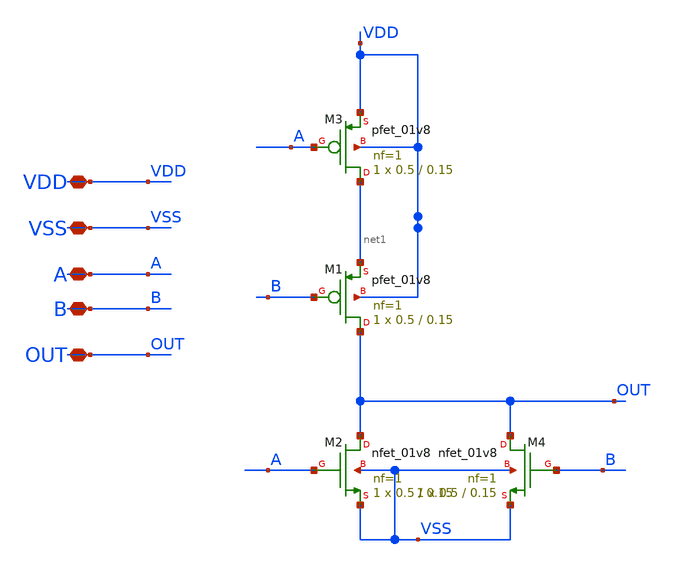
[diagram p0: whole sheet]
** sch_path: xschem/DC_DC_Converter_xschem/OTHERS/DC_DC_Converter_JV11/DELAY_JAWAD/NOR.sch
**.subckt NOR VDD VSS A B OUT
*.iopin VDD
*.iopin VSS
*.iopin A
*.iopin B
*.iopin OUT
XM2 OUT A VSS VSS sky130_fd_pr__nfet_01v8 L=0.15 W=0.5 nf=1 ad='int((nf+1)/2) * W/nf * 0.29' as='int((nf+2)/2) * W/nf * 0.29'
+ pd='2*int((nf+1)/2) * (W/nf + 0.29)' ps='2*int((nf+2)/2) * (W/nf + 0.29)' nrd='0.29 / W' nrs='0.29 / W'
+ sa=0 sb=0 sd=0 mult=1 m=1
XM3 net1 A VDD VDD sky130_fd_pr__pfet_01v8 L=0.15 W=0.5 nf=1 ad='int((nf+1)/2) * W/nf * 0.29' as='int((nf+2)/2) * W/nf * 0.29'
+ pd='2*int((nf+1)/2) * (W/nf + 0.29)' ps='2*int((nf+2)/2) * (W/nf + 0.29)' nrd='0.29 / W' nrs='0.29 / W'
+ sa=0 sb=0 sd=0 mult=1 m=1
XM1 OUT B net1 VDD sky130_fd_pr__pfet_01v8 L=0.15 W=0.5 nf=1 ad='int((nf+1)/2) * W/nf * 0.29' as='int((nf+2)/2) * W/nf * 0.29'
+ pd='2*int((nf+1)/2) * (W/nf + 0.29)' ps='2*int((nf+2)/2) * (W/nf + 0.29)' nrd='0.29 / W' nrs='0.29 / W'
+ sa=0 sb=0 sd=0 mult=1 m=1
XM4 OUT B VSS VSS sky130_fd_pr__nfet_01v8 L=0.15 W=0.5 nf=1 ad='int((nf+1)/2) * W/nf * 0.29' as='int((nf+2)/2) * W/nf * 0.29'
+ pd='2*int((nf+1)/2) * (W/nf + 0.29)' ps='2*int((nf+2)/2) * (W/nf + 0.29)' nrd='0.29 / W' nrs='0.29 / W'
+ sa=0 sb=0 sd=0 mult=1 m=1
**.ends
.end
